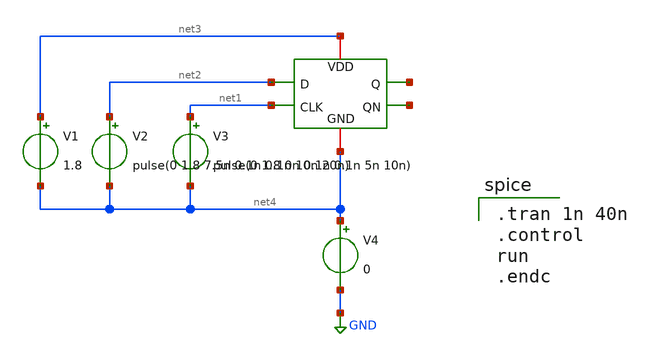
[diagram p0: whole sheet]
** sch_path: DFF_Test.sch
**.subckt DFF_Test
V1 net3 net4 1.8
V2 net2 net4 pulse(0 1.8 7.5n 0.1n 0.1n 10n 20n)
V3 net1 net4 pulse(0 1.8 0n 0.1n 0.1n 5n 10n)
V4 net4 GND 0
x1 net3 net2 net5 net6 net1 net4 DFlipFlop
**** begin user architecture code
 .lib $::SKYWATER_MODELS/sky130.lib.spice tt

.tran 1n 40n
.control
run
.endc

**** end user architecture code
**.ends
.GLOBAL GND
.end
